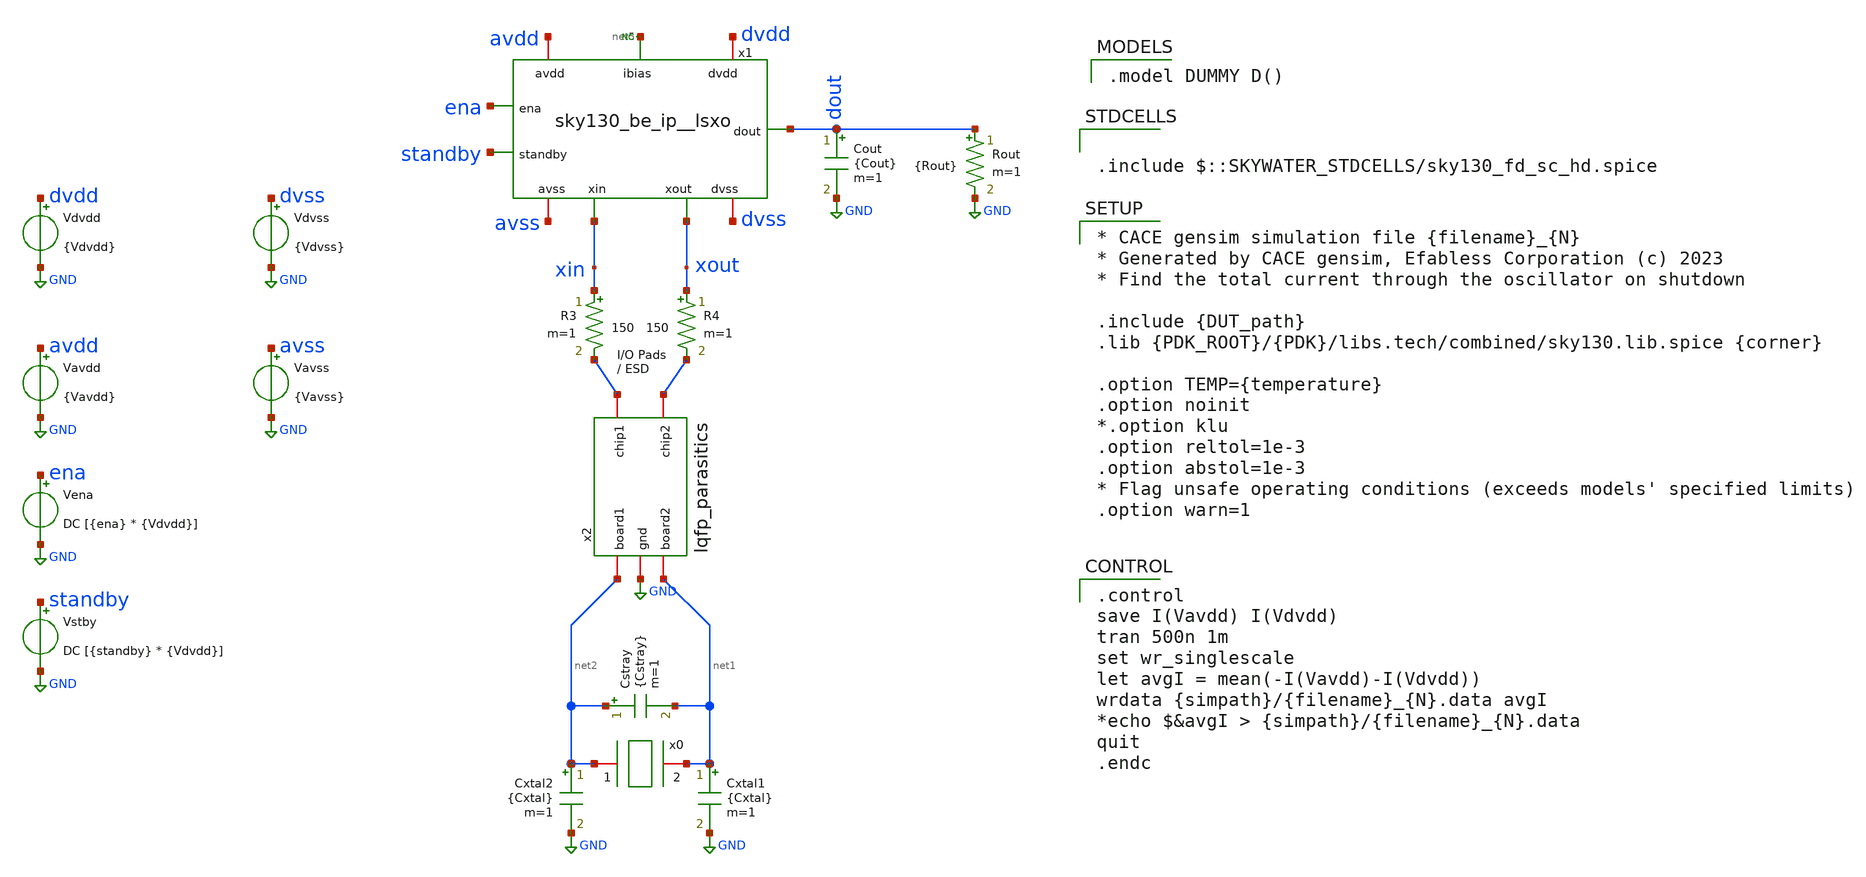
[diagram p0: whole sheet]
** sch_path: cace/tb_current_total.sch

.include $::SKYWATER_STDCELLS/sky130_fd_sc_hd.spice

**.subckt tb_current_total
Vdvdd dvdd GND {Vdvdd}
Vavdd avdd GND {Vavdd}
Cxtal2 net2 GND {Cxtal} m=1
Cxtal1 net1 GND {Cxtal} m=1
Cstray net2 net1 {Cstray} m=1
Cout dout GND {Cout} m=1
Vstby standby GND DC [{standby} * {Vdvdd}]
R3 xin net3 150 m=1
R4 xout net4 150 m=1
x2 net4 net3 GND net2 net1 lqfp_parasitics
Vena ena GND DC [{ena} * {Vdvdd}]
x1 avdd avss dvdd dvss net5 ena standby dout xin xout sky130_be_ip__lsxo
Vdvss dvss GND {Vdvss}
Vavss avss GND {Vavss}
Rout dout GND {Rout} m=1
x0 net2 net1 xtal_iqd_125_1
* noconn #net5
**** begin user architecture code

.model DUMMY D()


.control
save I(Vavdd) I(Vdvdd)
tran 500n 1m
set wr_singlescale
let avgI = mean(-I(Vavdd)-I(Vdvdd))
wrdata {simpath}/{filename}_{N}.data avgI
*echo $&avgI > {simpath}/{filename}_{N}.data
quit
.endc



* CACE gensim simulation file {filename}_{N}
* Generated by CACE gensim, Efabless Corporation (c) 2023
* Find the total current through the oscillator on shutdown

.include {DUT_path}
.lib {PDK_ROOT}/{PDK}/libs.tech/combined/sky130.lib.spice {corner}

.option TEMP={temperature}
.option noinit
*.option klu
.option reltol=1e-3
.option abstol=1e-3
* Flag unsafe operating conditions (exceeds models' specified limits)
.option warn=1


**** end user architecture code
**.ends
.GLOBAL GND
.end
